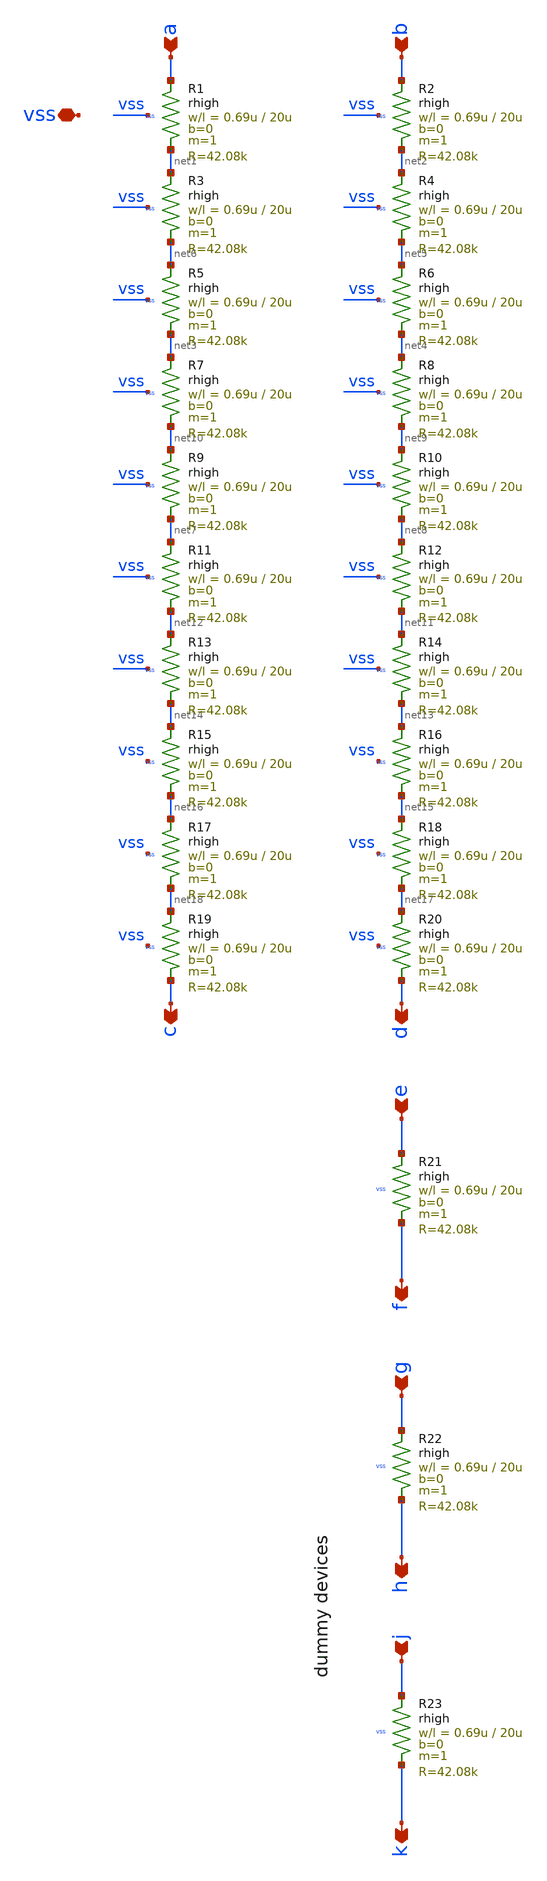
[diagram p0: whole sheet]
** sch_path: xschem/bg_res.sch
**.subckt bg_res a b c d vss f e h g k j
*.ipin a
*.ipin b
*.opin c
*.opin d
*.iopin vss
*.opin f
*.ipin e
*.opin h
*.ipin g
*.opin k
*.ipin j
XR1 a net1 vss rhigh w=0.69u l=20u m=1 b=0 mm_ok=1
XR2 b net2 vss rhigh w=0.69u l=20u m=1 b=0 mm_ok=1
XR3 net1 net6 vss rhigh w=0.69u l=20u m=1 b=0 mm_ok=1
XR4 net2 net5 vss rhigh w=0.69u l=20u m=1 b=0 mm_ok=1
XR5 net6 net3 vss rhigh w=0.69u l=20u m=1 b=0 mm_ok=1
XR6 net5 net4 vss rhigh w=0.69u l=20u m=1 b=0 mm_ok=1
XR7 net3 net10 vss rhigh w=0.69u l=20u m=1 b=0 mm_ok=1
XR8 net4 net9 vss rhigh w=0.69u l=20u m=1 b=0 mm_ok=1
XR9 net10 net7 vss rhigh w=0.69u l=20u m=1 b=0 mm_ok=1
XR10 net9 net8 vss rhigh w=0.69u l=20u m=1 b=0 mm_ok=1
XR11 net7 net12 vss rhigh w=0.69u l=20u m=1 b=0 mm_ok=1
XR12 net8 net11 vss rhigh w=0.69u l=20u m=1 b=0 mm_ok=1
XR13 net12 net14 vss rhigh w=0.69u l=20u m=1 b=0 mm_ok=1
XR14 net11 net13 vss rhigh w=0.69u l=20u m=1 b=0 mm_ok=1
XR15 net14 net16 vss rhigh w=0.69u l=20u m=1 b=0 mm_ok=1
XR16 net13 net15 vss rhigh w=0.69u l=20u m=1 b=0 mm_ok=1
XR17 net16 net18 vss rhigh w=0.69u l=20u m=1 b=0 mm_ok=1
XR18 net15 net17 vss rhigh w=0.69u l=20u m=1 b=0 mm_ok=1
XR19 net18 c vss rhigh w=0.69u l=20u m=1 b=0 mm_ok=1
XR20 net17 d vss rhigh w=0.69u l=20u m=1 b=0 mm_ok=1
XR21 e f vss rhigh w=0.69u l=20u m=1 b=0 mm_ok=1
XR22 g h vss rhigh w=0.69u l=20u m=1 b=0 mm_ok=1
XR23 j k vss rhigh w=0.69u l=20u m=1 b=0 mm_ok=1
**.ends
.end
